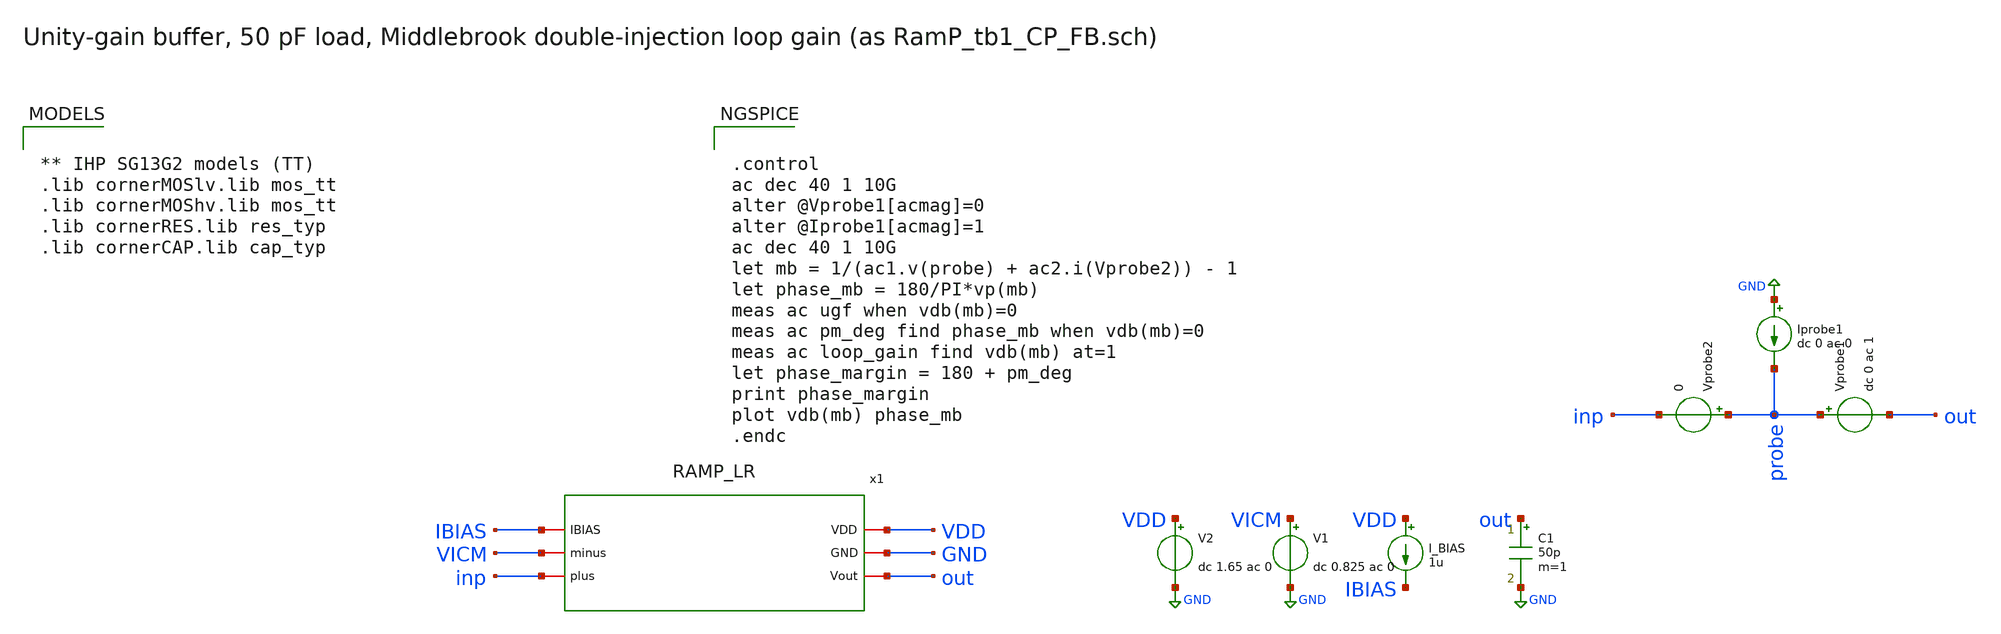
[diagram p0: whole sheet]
** sch_path: Design Files/RAMP/RAMP-LR/tb_RAMP_LR.sch
**.subckt tb_RAMP_LR
x1 VDD GND IBIAS VICM inp out RAMP_LR
V2 VDD GND dc 1.65 ac 0
V1 VICM GND dc 0.825 ac 0
I_BIAS VDD IBIAS 1u
C1 out GND 50p m=1
Vprobe2 probe inp 0
Vprobe1 probe out dc 0 ac 1
Iprobe1 GND probe dc 0 ac 0
**** begin user architecture code


** IHP SG13G2 models (TT)
.lib cornerMOSlv.lib mos_tt
.lib cornerMOShv.lib mos_tt
.lib cornerRES.lib res_typ
.lib cornerCAP.lib cap_typ




.control
ac dec 40 1 10G
alter @Vprobe1[acmag]=0
alter @Iprobe1[acmag]=1
ac dec 40 1 10G
let mb = 1/(ac1.v(probe) + ac2.i(Vprobe2)) - 1
let phase_mb = 180/PI*vp(mb)
meas ac ugf when vdb(mb)=0
meas ac pm_deg find phase_mb when vdb(mb)=0
meas ac loop_gain find vdb(mb) at=1
let phase_margin = 180 + pm_deg
print phase_margin
plot vdb(mb) phase_mb
.endc


**** end user architecture code
**.ends
.GLOBAL GND
.end
